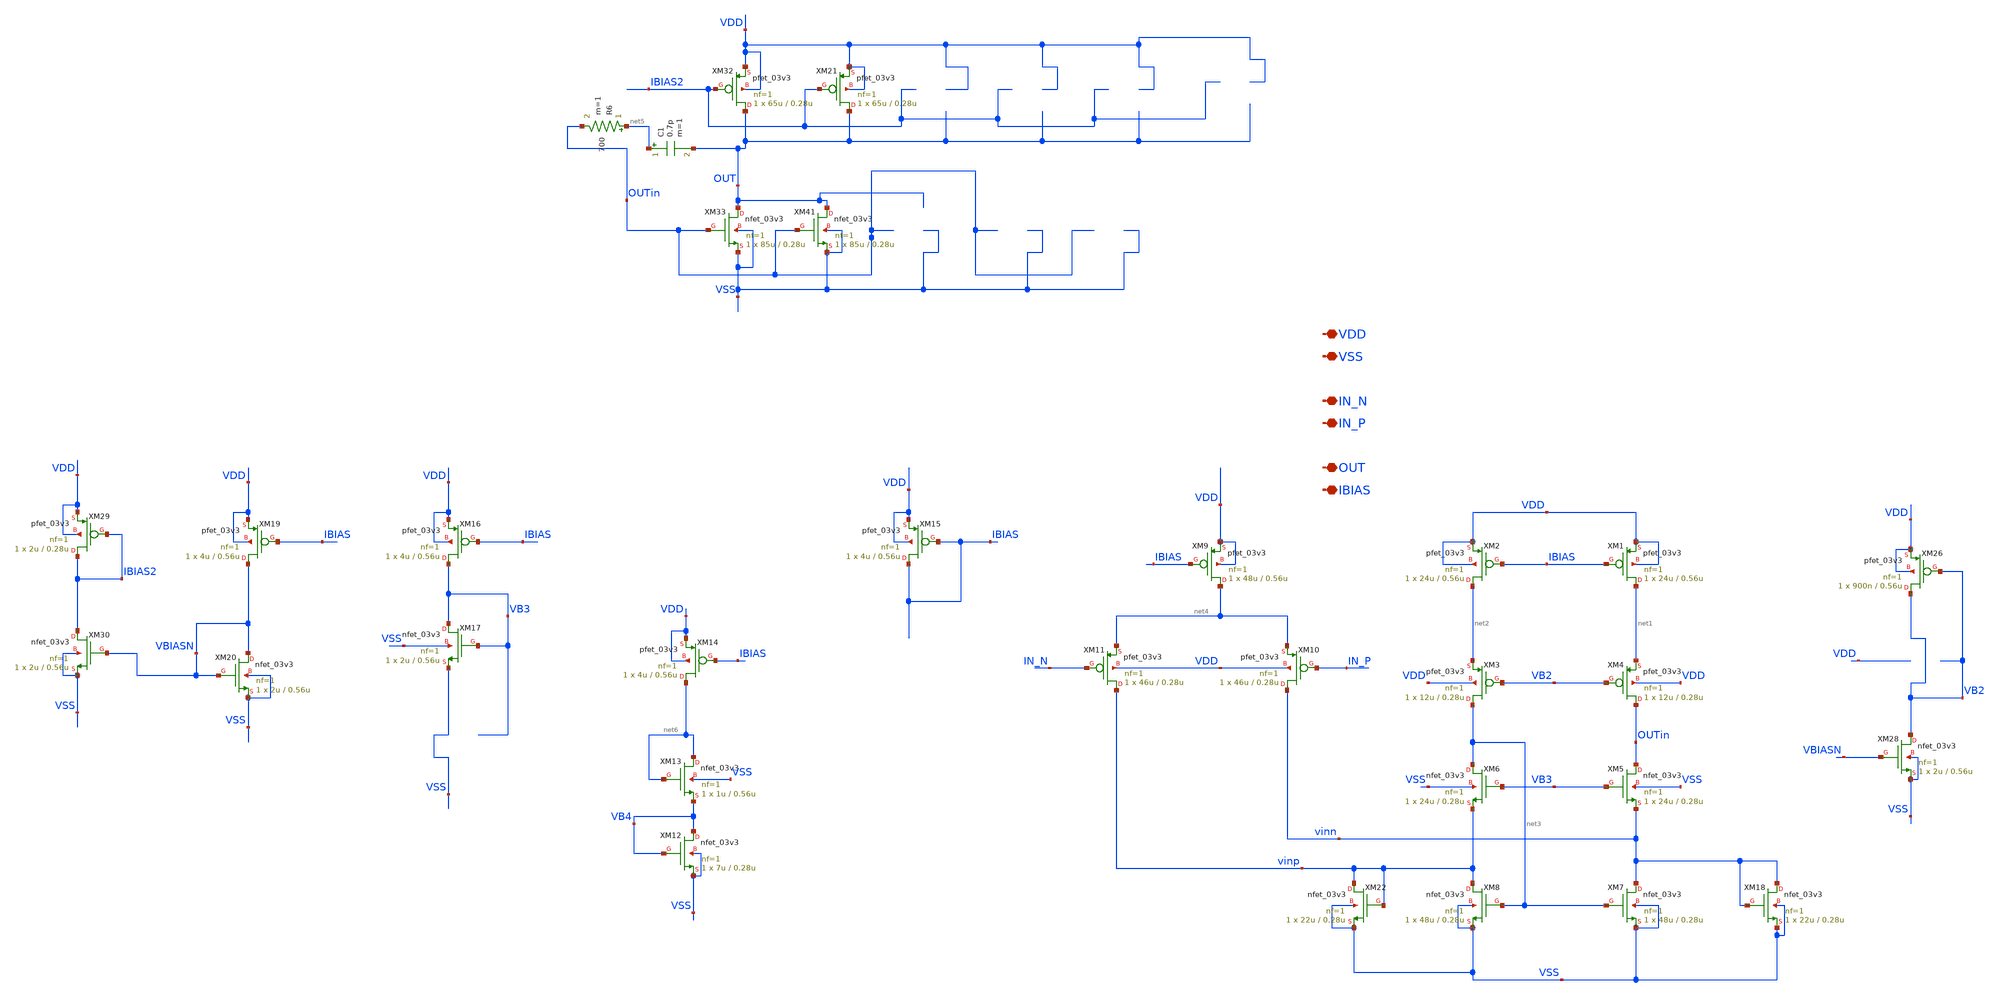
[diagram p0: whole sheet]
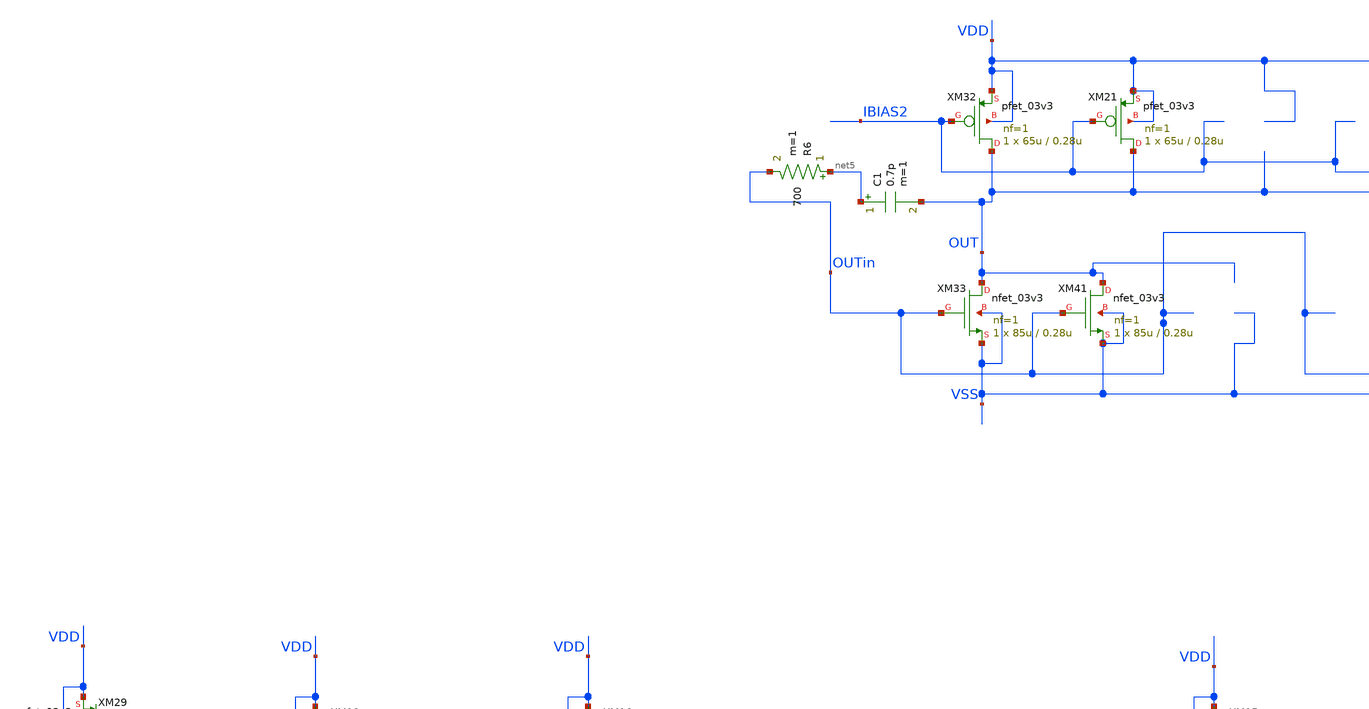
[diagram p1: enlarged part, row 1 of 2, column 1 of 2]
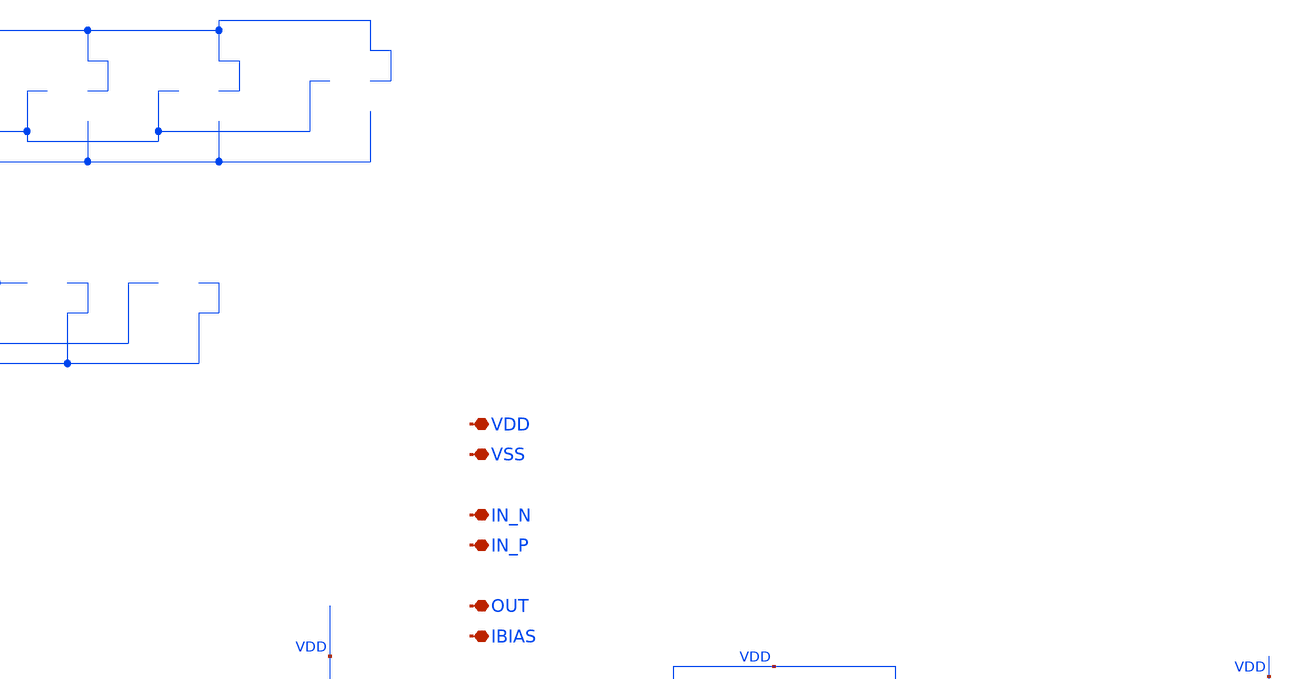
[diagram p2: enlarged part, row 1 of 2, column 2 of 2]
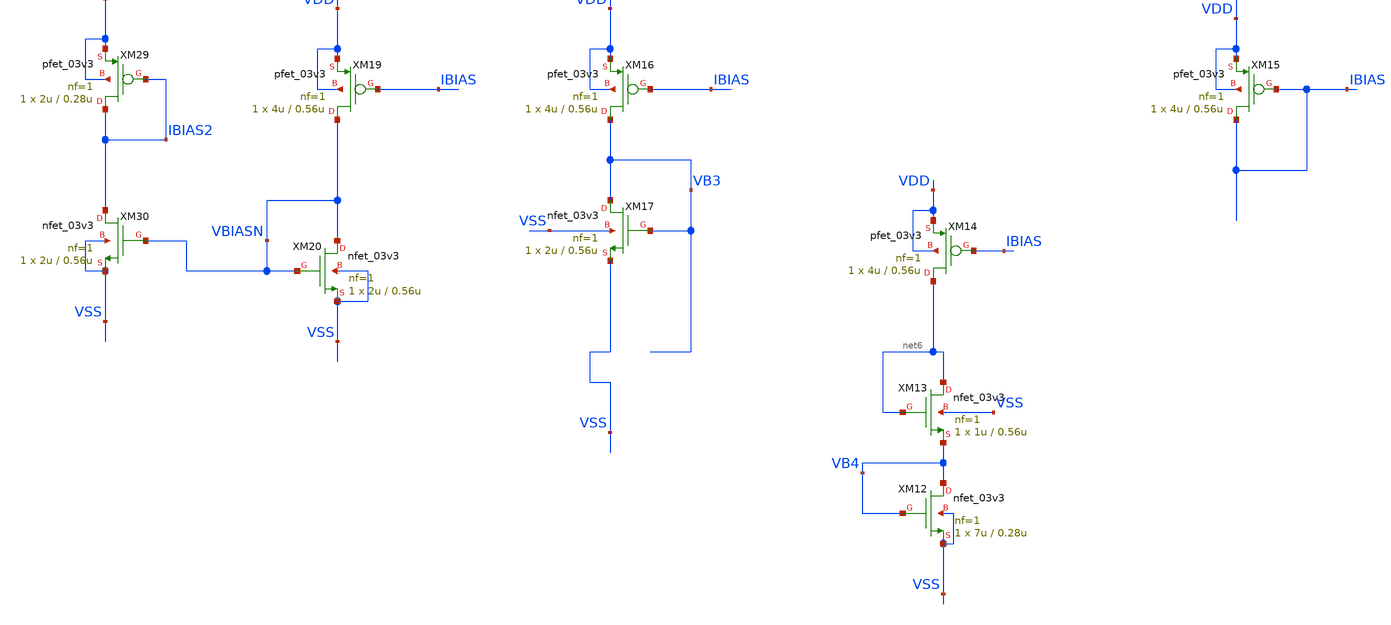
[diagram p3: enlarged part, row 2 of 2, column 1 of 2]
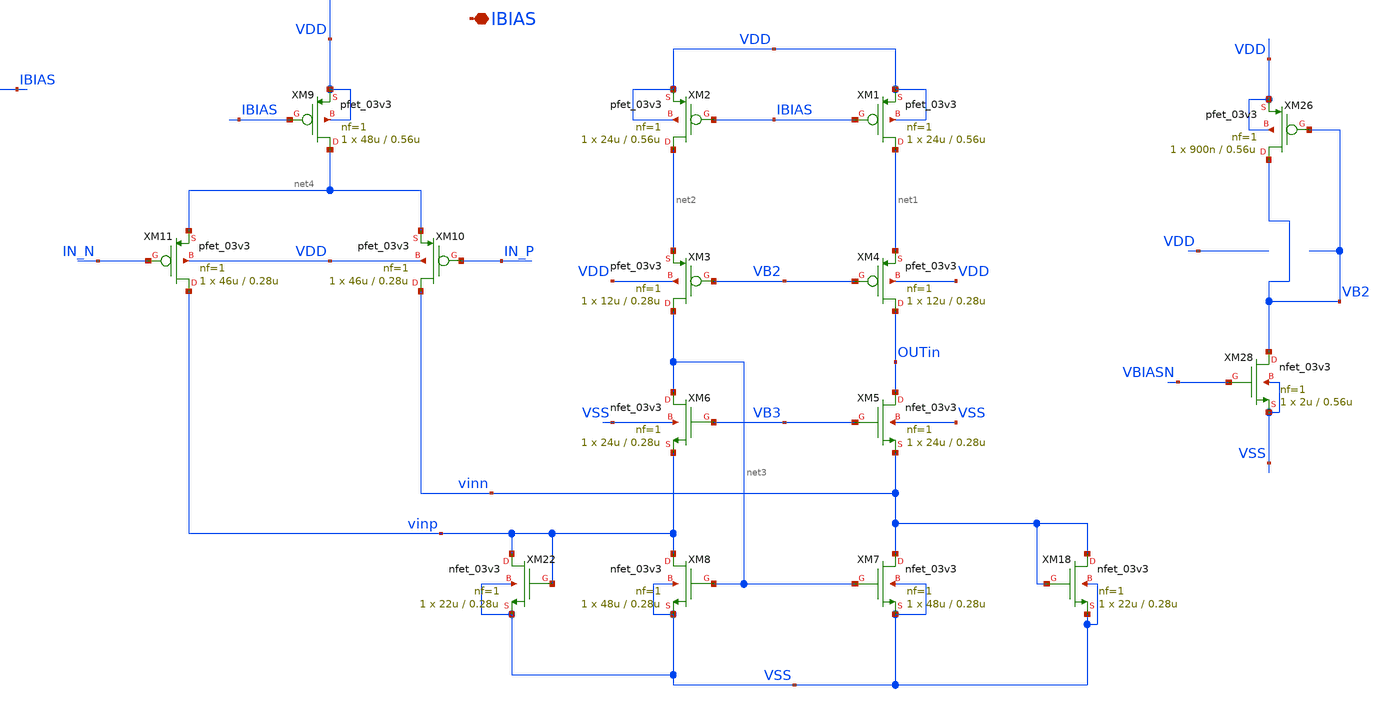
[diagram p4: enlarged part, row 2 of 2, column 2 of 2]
** sch_path: SCOP_INPUT_AND_MUX_PAKISTAN_03/Xschem/Folded_single/Folded_opamp_single.sch
**.subckt Folded_opamp_single VDD VSS IN_N IN_P OUT IBIAS
*.iopin VDD
*.iopin VSS
*.iopin IN_N
*.iopin IN_P
*.iopin OUT
*.iopin IBIAS
XM1 net1 IBIAS VDD VDD pfet_03v3 L=0.56u W=24u nf=1 ad='int((nf+1)/2) * W/nf * 0.18u' as='int((nf+2)/2) * W/nf * 0.18u'
+ pd='2*int((nf+1)/2) * (W/nf + 0.18u)' ps='2*int((nf+2)/2) * (W/nf + 0.18u)' nrd='0.18u / W' nrs='0.18u / W'
+ sa=0 sb=0 sd=0 m=1
XM2 net2 IBIAS VDD VDD pfet_03v3 L=0.56u W=24u nf=1 ad='int((nf+1)/2) * W/nf * 0.18u' as='int((nf+2)/2) * W/nf * 0.18u'
+ pd='2*int((nf+1)/2) * (W/nf + 0.18u)' ps='2*int((nf+2)/2) * (W/nf + 0.18u)' nrd='0.18u / W' nrs='0.18u / W'
+ sa=0 sb=0 sd=0 m=1
XM3 net3 VB2 net2 VDD pfet_03v3 L=0.28u W=12u nf=1 ad='int((nf+1)/2) * W/nf * 0.18u' as='int((nf+2)/2) * W/nf * 0.18u'
+ pd='2*int((nf+1)/2) * (W/nf + 0.18u)' ps='2*int((nf+2)/2) * (W/nf + 0.18u)' nrd='0.18u / W' nrs='0.18u / W'
+ sa=0 sb=0 sd=0 m=1
XM4 OUTin VB2 net1 VDD pfet_03v3 L=0.28u W=12u nf=1 ad='int((nf+1)/2) * W/nf * 0.18u' as='int((nf+2)/2) * W/nf * 0.18u'
+ pd='2*int((nf+1)/2) * (W/nf + 0.18u)' ps='2*int((nf+2)/2) * (W/nf + 0.18u)' nrd='0.18u / W' nrs='0.18u / W'
+ sa=0 sb=0 sd=0 m=1
XM5 OUTin VB3 vinn VSS nfet_03v3 L=0.28u W=24u nf=1 ad='int((nf+1)/2) * W/nf * 0.18u' as='int((nf+2)/2) * W/nf * 0.18u'
+ pd='2*int((nf+1)/2) * (W/nf + 0.18u)' ps='2*int((nf+2)/2) * (W/nf + 0.18u)' nrd='0.18u / W' nrs='0.18u / W'
+ sa=0 sb=0 sd=0 m=1
XM6 net3 VB3 vinp VSS nfet_03v3 L=0.28u W=24u nf=1 ad='int((nf+1)/2) * W/nf * 0.18u' as='int((nf+2)/2) * W/nf * 0.18u'
+ pd='2*int((nf+1)/2) * (W/nf + 0.18u)' ps='2*int((nf+2)/2) * (W/nf + 0.18u)' nrd='0.18u / W' nrs='0.18u / W'
+ sa=0 sb=0 sd=0 m=1
XM7 vinn net3 VSS VSS nfet_03v3 L=0.28u W=48u nf=1 ad='int((nf+1)/2) * W/nf * 0.18u' as='int((nf+2)/2) * W/nf * 0.18u'
+ pd='2*int((nf+1)/2) * (W/nf + 0.18u)' ps='2*int((nf+2)/2) * (W/nf + 0.18u)' nrd='0.18u / W' nrs='0.18u / W'
+ sa=0 sb=0 sd=0 m=1
XM8 vinp net3 VSS VSS nfet_03v3 L=0.28u W=48u nf=1 ad='int((nf+1)/2) * W/nf * 0.18u' as='int((nf+2)/2) * W/nf * 0.18u'
+ pd='2*int((nf+1)/2) * (W/nf + 0.18u)' ps='2*int((nf+2)/2) * (W/nf + 0.18u)' nrd='0.18u / W' nrs='0.18u / W'
+ sa=0 sb=0 sd=0 m=1
XM9 net4 IBIAS VDD VDD pfet_03v3 L=0.56u W=48u nf=1 ad='int((nf+1)/2) * W/nf * 0.18u' as='int((nf+2)/2) * W/nf * 0.18u'
+ pd='2*int((nf+1)/2) * (W/nf + 0.18u)' ps='2*int((nf+2)/2) * (W/nf + 0.18u)' nrd='0.18u / W' nrs='0.18u / W'
+ sa=0 sb=0 sd=0 m=1
XM10 vinn IN_P net4 VDD pfet_03v3 L=0.28u W=46u nf=1 ad='int((nf+1)/2) * W/nf * 0.18u' as='int((nf+2)/2) * W/nf * 0.18u'
+ pd='2*int((nf+1)/2) * (W/nf + 0.18u)' ps='2*int((nf+2)/2) * (W/nf + 0.18u)' nrd='0.18u / W' nrs='0.18u / W'
+ sa=0 sb=0 sd=0 m=1
XM11 vinp IN_N net4 VDD pfet_03v3 L=0.28u W=46u nf=1 ad='int((nf+1)/2) * W/nf * 0.18u' as='int((nf+2)/2) * W/nf * 0.18u'
+ pd='2*int((nf+1)/2) * (W/nf + 0.18u)' ps='2*int((nf+2)/2) * (W/nf + 0.18u)' nrd='0.18u / W' nrs='0.18u / W'
+ sa=0 sb=0 sd=0 m=1
XM15 IBIAS IBIAS VDD VDD pfet_03v3 L=0.56u W=4u nf=1 ad='int((nf+1)/2) * W/nf * 0.18u' as='int((nf+2)/2) * W/nf * 0.18u'
+ pd='2*int((nf+1)/2) * (W/nf + 0.18u)' ps='2*int((nf+2)/2) * (W/nf + 0.18u)' nrd='0.18u / W' nrs='0.18u / W'
+ sa=0 sb=0 sd=0 m=1
XM16 VB3 IBIAS VDD VDD pfet_03v3 L=0.56u W=4u nf=1 ad='int((nf+1)/2) * W/nf * 0.18u' as='int((nf+2)/2) * W/nf * 0.18u'
+ pd='2*int((nf+1)/2) * (W/nf + 0.18u)' ps='2*int((nf+2)/2) * (W/nf + 0.18u)' nrd='0.18u / W' nrs='0.18u / W'
+ sa=0 sb=0 sd=0 m=1
XM17 VB3 VB3 VSS VSS nfet_03v3 L=0.56u W=2u nf=1 ad='int((nf+1)/2) * W/nf * 0.18u' as='int((nf+2)/2) * W/nf * 0.18u'
+ pd='2*int((nf+1)/2) * (W/nf + 0.18u)' ps='2*int((nf+2)/2) * (W/nf + 0.18u)' nrd='0.18u / W' nrs='0.18u / W'
+ sa=0 sb=0 sd=0 m=1
XM19 VBIASN IBIAS VDD VDD pfet_03v3 L=0.56u W=4u nf=1 ad='int((nf+1)/2) * W/nf * 0.18u' as='int((nf+2)/2) * W/nf * 0.18u'
+ pd='2*int((nf+1)/2) * (W/nf + 0.18u)' ps='2*int((nf+2)/2) * (W/nf + 0.18u)' nrd='0.18u / W' nrs='0.18u / W'
+ sa=0 sb=0 sd=0 m=1
XM20 VBIASN VBIASN VSS VSS nfet_03v3 L=0.56u W=2u nf=1 ad='int((nf+1)/2) * W/nf * 0.18u' as='int((nf+2)/2) * W/nf * 0.18u'
+ pd='2*int((nf+1)/2) * (W/nf + 0.18u)' ps='2*int((nf+2)/2) * (W/nf + 0.18u)' nrd='0.18u / W' nrs='0.18u / W'
+ sa=0 sb=0 sd=0 m=1
XM26 VB2 VB2 VDD VDD pfet_03v3 L=0.56u W=900n nf=1 ad='int((nf+1)/2) * W/nf * 0.18u' as='int((nf+2)/2) * W/nf * 0.18u'
+ pd='2*int((nf+1)/2) * (W/nf + 0.18u)' ps='2*int((nf+2)/2) * (W/nf + 0.18u)' nrd='0.18u / W' nrs='0.18u / W'
+ sa=0 sb=0 sd=0 m=1
XM28 VB2 VBIASN VSS VSS nfet_03v3 L=0.56u W=2u nf=1 ad='int((nf+1)/2) * W/nf * 0.18u' as='int((nf+2)/2) * W/nf * 0.18u'
+ pd='2*int((nf+1)/2) * (W/nf + 0.18u)' ps='2*int((nf+2)/2) * (W/nf + 0.18u)' nrd='0.18u / W' nrs='0.18u / W'
+ sa=0 sb=0 sd=0 m=1
XM29 IBIAS2 IBIAS2 VDD VDD pfet_03v3 L=0.28u W=2u nf=1 ad='int((nf+1)/2) * W/nf * 0.18u' as='int((nf+2)/2) * W/nf * 0.18u'
+ pd='2*int((nf+1)/2) * (W/nf + 0.18u)' ps='2*int((nf+2)/2) * (W/nf + 0.18u)' nrd='0.18u / W' nrs='0.18u / W'
+ sa=0 sb=0 sd=0 m=1
XM30 IBIAS2 VBIASN VSS VSS nfet_03v3 L=0.56u W=2u nf=1 ad='int((nf+1)/2) * W/nf * 0.18u' as='int((nf+2)/2) * W/nf * 0.18u'
+ pd='2*int((nf+1)/2) * (W/nf + 0.18u)' ps='2*int((nf+2)/2) * (W/nf + 0.18u)' nrd='0.18u / W' nrs='0.18u / W'
+ sa=0 sb=0 sd=0 m=1
XM32 OUT IBIAS2 VDD VDD pfet_03v3 L=0.28u W=65u nf=1 ad='int((nf+1)/2) * W/nf * 0.18u' as='int((nf+2)/2) * W/nf * 0.18u'
+ pd='2*int((nf+1)/2) * (W/nf + 0.18u)' ps='2*int((nf+2)/2) * (W/nf + 0.18u)' nrd='0.18u / W' nrs='0.18u / W'
+ sa=0 sb=0 sd=0 m=1
XM33 OUT OUTin VSS VSS nfet_03v3 L=0.28u W=85u nf=1 ad='int((nf+1)/2) * W/nf * 0.18u' as='int((nf+2)/2) * W/nf * 0.18u'
+ pd='2*int((nf+1)/2) * (W/nf + 0.18u)' ps='2*int((nf+2)/2) * (W/nf + 0.18u)' nrd='0.18u / W' nrs='0.18u / W'
+ sa=0 sb=0 sd=0 m=1
R6 net5 OUTin 700 m=1
XM41 OUT OUTin VSS VSS nfet_03v3 L=0.28u W=85u nf=1 ad='int((nf+1)/2) * W/nf * 0.18u' as='int((nf+2)/2) * W/nf * 0.18u'
+ pd='2*int((nf+1)/2) * (W/nf + 0.18u)' ps='2*int((nf+2)/2) * (W/nf + 0.18u)' nrd='0.18u / W' nrs='0.18u / W'
+ sa=0 sb=0 sd=0 m=1
XM12 VB4 VB4 VSS VSS nfet_03v3 L=0.28u W=7u nf=1 ad='int((nf+1)/2) * W/nf * 0.18u' as='int((nf+2)/2) * W/nf * 0.18u'
+ pd='2*int((nf+1)/2) * (W/nf + 0.18u)' ps='2*int((nf+2)/2) * (W/nf + 0.18u)' nrd='0.18u / W' nrs='0.18u / W'
+ sa=0 sb=0 sd=0 m=1
XM13 net6 net6 VB4 VSS nfet_03v3 L=0.56u W=1u nf=1 ad='int((nf+1)/2) * W/nf * 0.18u' as='int((nf+2)/2) * W/nf * 0.18u'
+ pd='2*int((nf+1)/2) * (W/nf + 0.18u)' ps='2*int((nf+2)/2) * (W/nf + 0.18u)' nrd='0.18u / W' nrs='0.18u / W'
+ sa=0 sb=0 sd=0 m=1
XM14 net6 IBIAS VDD VDD pfet_03v3 L=0.56u W=4u nf=1 ad='int((nf+1)/2) * W/nf * 0.18u' as='int((nf+2)/2) * W/nf * 0.18u'
+ pd='2*int((nf+1)/2) * (W/nf + 0.18u)' ps='2*int((nf+2)/2) * (W/nf + 0.18u)' nrd='0.18u / W' nrs='0.18u / W'
+ sa=0 sb=0 sd=0 m=1
XM21 OUT IBIAS2 VDD VDD pfet_03v3 L=0.28u W=65u nf=1 ad='int((nf+1)/2) * W/nf * 0.18u' as='int((nf+2)/2) * W/nf * 0.18u'
+ pd='2*int((nf+1)/2) * (W/nf + 0.18u)' ps='2*int((nf+2)/2) * (W/nf + 0.18u)' nrd='0.18u / W' nrs='0.18u / W'
+ sa=0 sb=0 sd=0 m=1
C1 net5 OUT 0.7p m=1
XM18 vinn vinn VSS VSS nfet_03v3 L=0.28u W=22u nf=1 ad='int((nf+1)/2) * W/nf * 0.18u' as='int((nf+2)/2) * W/nf * 0.18u'
+ pd='2*int((nf+1)/2) * (W/nf + 0.18u)' ps='2*int((nf+2)/2) * (W/nf + 0.18u)' nrd='0.18u / W' nrs='0.18u / W'
+ sa=0 sb=0 sd=0 m=1
XM22 vinp vinp VSS VSS nfet_03v3 L=0.28u W=22u nf=1 ad='int((nf+1)/2) * W/nf * 0.18u' as='int((nf+2)/2) * W/nf * 0.18u'
+ pd='2*int((nf+1)/2) * (W/nf + 0.18u)' ps='2*int((nf+2)/2) * (W/nf + 0.18u)' nrd='0.18u / W' nrs='0.18u / W'
+ sa=0 sb=0 sd=0 m=1
**.ends
.end
